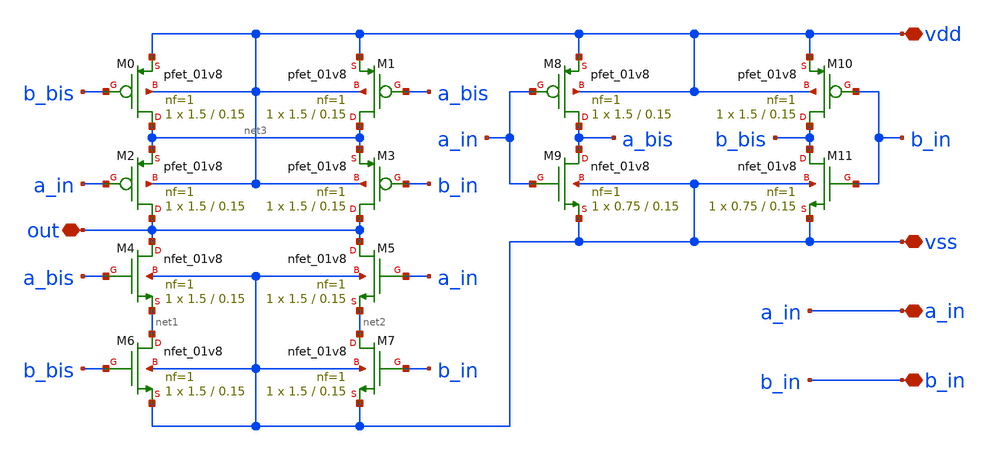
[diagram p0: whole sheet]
** sch_path: design/blocks/xorgate/schematic/xorgate.sch
**.subckt xorgate out vdd vss a_in b_in
*.iopin out
*.iopin vdd
*.iopin vss
*.iopin a_in
*.iopin b_in
XM0 net3 b_bis vdd vdd sky130_fd_pr__pfet_01v8 L=0.15 W=1.5 nf=1 ad='int((nf+1)/2) * W/nf * 0.29' as='int((nf+2)/2) * W/nf * 0.29'
+ pd='2*int((nf+1)/2) * (W/nf + 0.29)' ps='2*int((nf+2)/2) * (W/nf + 0.29)' nrd='0.29 / W' nrs='0.29 / W'
+ sa=0 sb=0 sd=0 mult=1 m=1
XM1 net3 a_bis vdd vdd sky130_fd_pr__pfet_01v8 L=0.15 W=1.5 nf=1 ad='int((nf+1)/2) * W/nf * 0.29' as='int((nf+2)/2) * W/nf * 0.29'
+ pd='2*int((nf+1)/2) * (W/nf + 0.29)' ps='2*int((nf+2)/2) * (W/nf + 0.29)' nrd='0.29 / W' nrs='0.29 / W'
+ sa=0 sb=0 sd=0 mult=1 m=1
XM2 out a_in net3 vdd sky130_fd_pr__pfet_01v8 L=0.15 W=1.5 nf=1 ad='int((nf+1)/2) * W/nf * 0.29' as='int((nf+2)/2) * W/nf * 0.29'
+ pd='2*int((nf+1)/2) * (W/nf + 0.29)' ps='2*int((nf+2)/2) * (W/nf + 0.29)' nrd='0.29 / W' nrs='0.29 / W'
+ sa=0 sb=0 sd=0 mult=1 m=1
XM3 out b_in net3 vdd sky130_fd_pr__pfet_01v8 L=0.15 W=1.5 nf=1 ad='int((nf+1)/2) * W/nf * 0.29' as='int((nf+2)/2) * W/nf * 0.29'
+ pd='2*int((nf+1)/2) * (W/nf + 0.29)' ps='2*int((nf+2)/2) * (W/nf + 0.29)' nrd='0.29 / W' nrs='0.29 / W'
+ sa=0 sb=0 sd=0 mult=1 m=1
XM4 out a_bis net1 vss sky130_fd_pr__nfet_01v8 L=0.15 W=1.5 nf=1 ad='int((nf+1)/2) * W/nf * 0.29' as='int((nf+2)/2) * W/nf * 0.29'
+ pd='2*int((nf+1)/2) * (W/nf + 0.29)' ps='2*int((nf+2)/2) * (W/nf + 0.29)' nrd='0.29 / W' nrs='0.29 / W'
+ sa=0 sb=0 sd=0 mult=1 m=1
XM5 out a_in net2 vss sky130_fd_pr__nfet_01v8 L=0.15 W=1.5 nf=1 ad='int((nf+1)/2) * W/nf * 0.29' as='int((nf+2)/2) * W/nf * 0.29'
+ pd='2*int((nf+1)/2) * (W/nf + 0.29)' ps='2*int((nf+2)/2) * (W/nf + 0.29)' nrd='0.29 / W' nrs='0.29 / W'
+ sa=0 sb=0 sd=0 mult=1 m=1
XM6 net1 b_bis vss vss sky130_fd_pr__nfet_01v8 L=0.15 W=1.5 nf=1 ad='int((nf+1)/2) * W/nf * 0.29' as='int((nf+2)/2) * W/nf * 0.29'
+ pd='2*int((nf+1)/2) * (W/nf + 0.29)' ps='2*int((nf+2)/2) * (W/nf + 0.29)' nrd='0.29 / W' nrs='0.29 / W'
+ sa=0 sb=0 sd=0 mult=1 m=1
XM7 net2 b_in vss vss sky130_fd_pr__nfet_01v8 L=0.15 W=1.5 nf=1 ad='int((nf+1)/2) * W/nf * 0.29' as='int((nf+2)/2) * W/nf * 0.29'
+ pd='2*int((nf+1)/2) * (W/nf + 0.29)' ps='2*int((nf+2)/2) * (W/nf + 0.29)' nrd='0.29 / W' nrs='0.29 / W'
+ sa=0 sb=0 sd=0 mult=1 m=1
XM8 a_bis a_in vdd vdd sky130_fd_pr__pfet_01v8 L=0.15 W=1.5 nf=1 ad='int((nf+1)/2) * W/nf * 0.29' as='int((nf+2)/2) * W/nf * 0.29'
+ pd='2*int((nf+1)/2) * (W/nf + 0.29)' ps='2*int((nf+2)/2) * (W/nf + 0.29)' nrd='0.29 / W' nrs='0.29 / W'
+ sa=0 sb=0 sd=0 mult=1 m=1
XM9 a_bis a_in vss vss sky130_fd_pr__nfet_01v8 L=0.15 W=0.75 nf=1 ad='int((nf+1)/2) * W/nf * 0.29' as='int((nf+2)/2) * W/nf * 0.29'
+ pd='2*int((nf+1)/2) * (W/nf + 0.29)' ps='2*int((nf+2)/2) * (W/nf + 0.29)' nrd='0.29 / W' nrs='0.29 / W'
+ sa=0 sb=0 sd=0 mult=1 m=1
XM10 b_bis b_in vdd vdd sky130_fd_pr__pfet_01v8 L=0.15 W=1.5 nf=1 ad='int((nf+1)/2) * W/nf * 0.29' as='int((nf+2)/2) * W/nf * 0.29'
+ pd='2*int((nf+1)/2) * (W/nf + 0.29)' ps='2*int((nf+2)/2) * (W/nf + 0.29)' nrd='0.29 / W' nrs='0.29 / W'
+ sa=0 sb=0 sd=0 mult=1 m=1
XM11 b_bis b_in vss vss sky130_fd_pr__nfet_01v8 L=0.15 W=0.75 nf=1 ad='int((nf+1)/2) * W/nf * 0.29' as='int((nf+2)/2) * W/nf * 0.29'
+ pd='2*int((nf+1)/2) * (W/nf + 0.29)' ps='2*int((nf+2)/2) * (W/nf + 0.29)' nrd='0.29 / W' nrs='0.29 / W'
+ sa=0 sb=0 sd=0 mult=1 m=1
**.ends
.end
